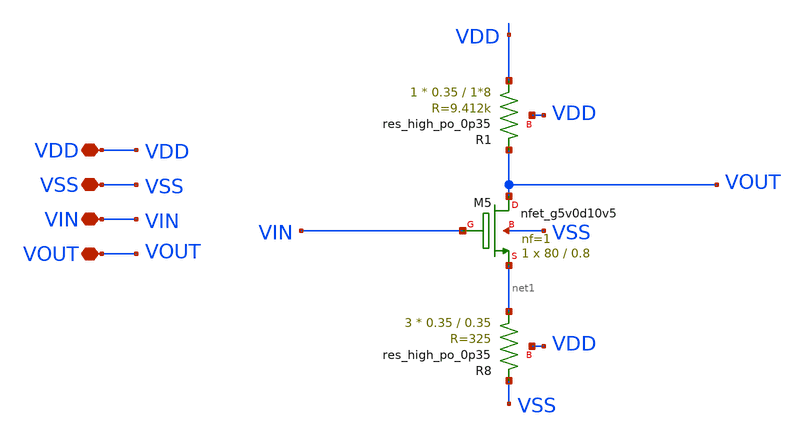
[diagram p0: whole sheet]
** sch_path: old stuff/amplifiers/single_stage_amps/basic_stages/cs_degenerated/cs_degenerated_stage.sch
**.subckt cs_degenerated_stage VDD VSS VIN VOUT
*.iopin VDD
*.iopin VSS
*.iopin VIN
*.iopin VOUT
XR1 VDD VOUT VDD sky130_fd_pr__res_high_po_0p35 L=1*8 mult=1 m=1
XR8 net1 VSS VDD sky130_fd_pr__res_high_po_0p35 L=0.35 mult=3 m=3
XM5 VOUT VIN net1 VSS sky130_fd_pr__nfet_g5v0d10v5 L=0.8 W=80 nf=1 ad='int((1 + 1)/2) * 80 / 1 * 0.29'
+ as='int((1 + 2)/2) * 80 / 1 * 0.29' pd='2*int((1 + 1)/2) * (80 / 1 + 0.29)' ps='2*int((1 + 2)/2) * (80 / 1 + 0.29)'
+ nrd='0.29 / 80 ' nrs='0.29 / 80 ' sa=0 sb=0 sd=0 mult=1 m=1
**.ends
.end
